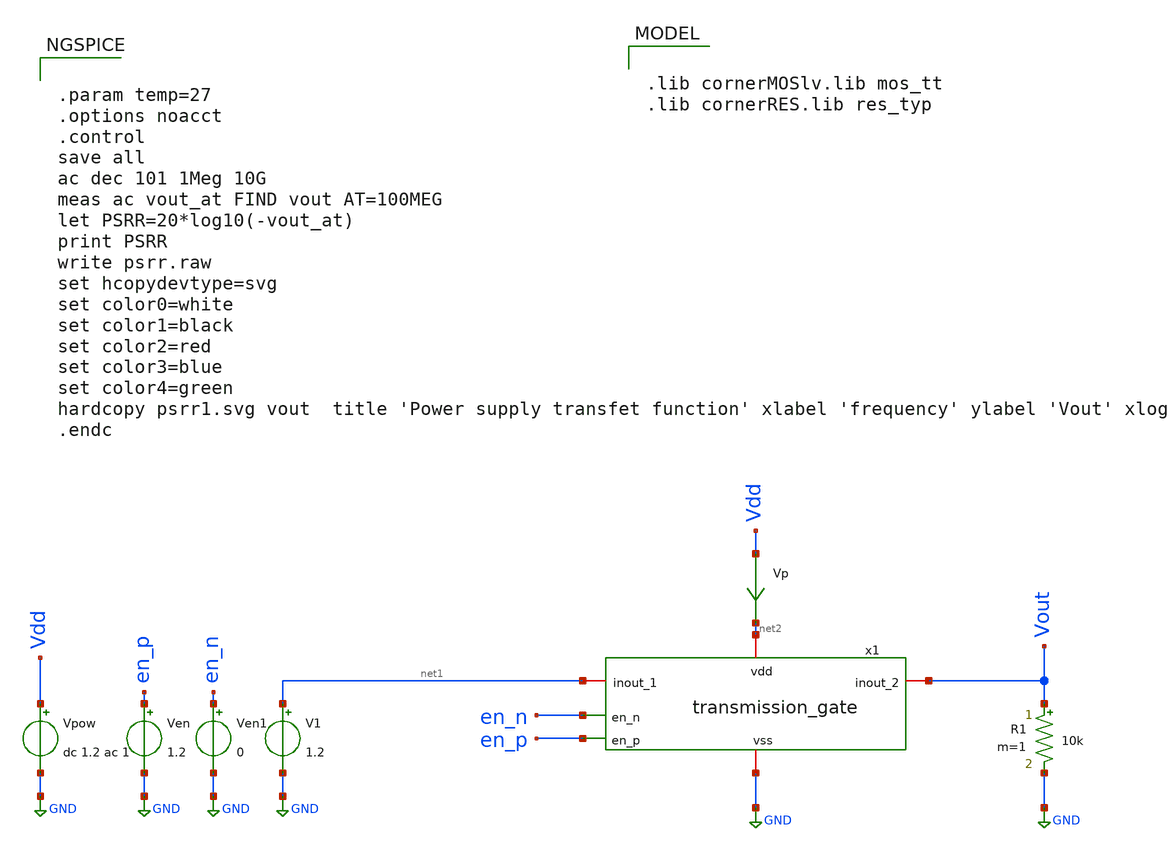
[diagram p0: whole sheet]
** sch_path: CHIPCHILE_CANELOS24_WorkshopTO/design_data/xschem/tgate/transmission_gate_tb_PSRR.sch
* Copyright 2023 IHP PDK Authors
**.subckt transmission_gate_tb_PSRR
Vpow Vdd GND dc 1.2 ac 1
Vp Vdd net2 0
.save i(vp)
Ven en_p GND 1.2
Ven1 en_n GND 0
x1 net2 en_n net1 Vout en_p GND transmission_gate
V1 net1 GND 1.2
R1 Vout GND 10k m=1
**** begin user architecture code

.lib cornerMOSlv.lib mos_tt
.lib cornerRES.lib res_typ



.param temp=27
.options noacct
.control
save all
ac dec 101 1Meg 10G
meas ac vout_at FIND vout AT=100MEG
let PSRR=20*log10(-vout_at)
print PSRR
write psrr.raw
set hcopydevtype=svg
set color0=white
set color1=black
set color2=red
set color3=blue
set color4=green
hardcopy psrr1.svg vout  title 'Power supply transfet function' xlabel 'frequency' ylabel 'Vout' xlog
.endc


**** end user architecture code
**.ends

* expanding   symbol:  transmission_gate.sym # of pins=6
** sym_path: CHIPCHILE_CANELOS24_WorkshopTO/design_data/xschem/multiplexer/transmission_gate.sym
** sch_path: CHIPCHILE_CANELOS24_WorkshopTO/design_data/xschem/multiplexer/transmission_gate.sch
.subckt transmission_gate vdd en_n inout_1 inout_2 en_p vss
*.iopin inout_1
*.iopin inout_2
*.ipin en_p
*.iopin vdd
*.iopin vss
*.ipin en_n
XM1 inout_1 en_p inout_2 net1 sg13_lv_nmos w=200.0u l=0.130u ng=20 m=1 mm_ok=1
XM2 inout_1 en_n inout_2 net2 sg13_lv_pmos w=200.0u l=0.130u ng=20 m=1 mm_ok=1
XR1 vdd net2 ntap1 R=262.8 w=0.78e-6 l=0.78e-6
XR2 vss net1 ptap1 R=262.8 w=0.78e-6 l=0.78e-6
.ends

.GLOBAL GND
.end
